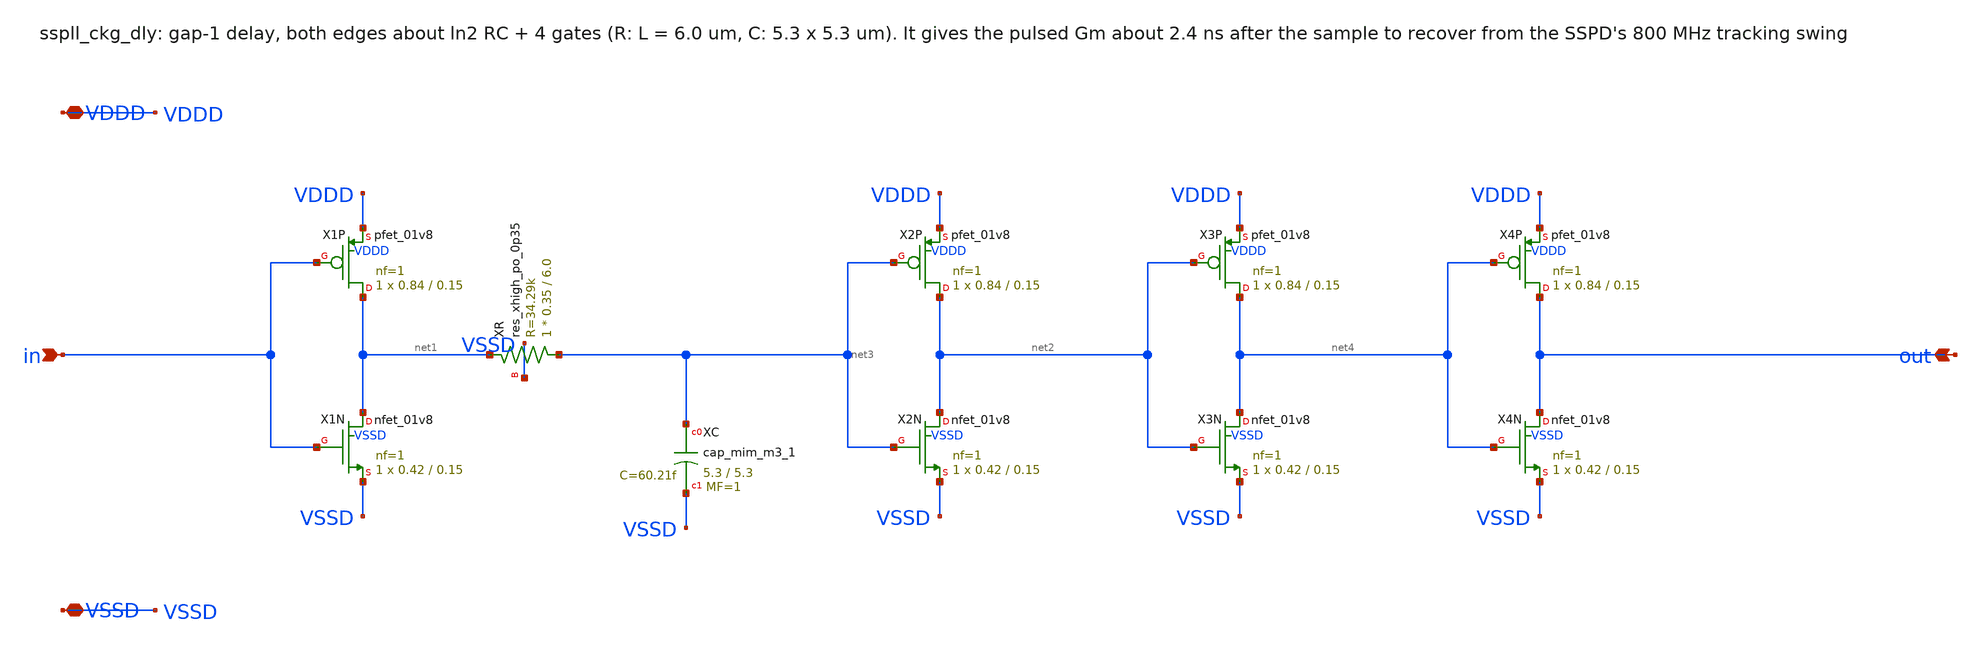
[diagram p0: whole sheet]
** sch_path: xschem/clkgen_hv/sspll_ckg_dly.sch
**.subckt sspll_ckg_dly in out VDDD VSSD
*.ipin in
*.opin out
*.iopin VDDD
*.iopin VSSD
XX1P net1 in VDDD VDDD sky130_fd_pr__pfet_01v8 L=0.15 W=0.84 nf=1 ad='int((nf+1)/2) * W/nf * 0.29' as='int((nf+2)/2) * W/nf * 0.29'
+ pd='2*int((nf+1)/2) * (W/nf + 0.29)' ps='2*int((nf+2)/2) * (W/nf + 0.29)' nrd='0.29 / W' nrs='0.29 / W'
+ sa=0 sb=0 sd=0 mult=1 m=1
XX1N net1 in VSSD VSSD sky130_fd_pr__nfet_01v8 L=0.15 W=0.42 nf=1 ad='int((nf+1)/2) * W/nf * 0.29' as='int((nf+2)/2) * W/nf * 0.29'
+ pd='2*int((nf+1)/2) * (W/nf + 0.29)' ps='2*int((nf+2)/2) * (W/nf + 0.29)' nrd='0.29 / W' nrs='0.29 / W'
+ sa=0 sb=0 sd=0 mult=1 m=1
XXR net3 net1 VSSD sky130_fd_pr__res_xhigh_po_0p35 L=6.0 mult=1 m=1
XXC net3 VSSD sky130_fd_pr__cap_mim_m3_1 W=5.3 L=5.3 MF=1 m=1
XX2P net2 net3 VDDD VDDD sky130_fd_pr__pfet_01v8 L=0.15 W=0.84 nf=1 ad='int((nf+1)/2) * W/nf * 0.29'
+ as='int((nf+2)/2) * W/nf * 0.29' pd='2*int((nf+1)/2) * (W/nf + 0.29)' ps='2*int((nf+2)/2) * (W/nf + 0.29)'
+ nrd='0.29 / W' nrs='0.29 / W' sa=0 sb=0 sd=0 mult=1 m=1
XX2N net2 net3 VSSD VSSD sky130_fd_pr__nfet_01v8 L=0.15 W=0.42 nf=1 ad='int((nf+1)/2) * W/nf * 0.29'
+ as='int((nf+2)/2) * W/nf * 0.29' pd='2*int((nf+1)/2) * (W/nf + 0.29)' ps='2*int((nf+2)/2) * (W/nf + 0.29)'
+ nrd='0.29 / W' nrs='0.29 / W' sa=0 sb=0 sd=0 mult=1 m=1
XX3P net4 net2 VDDD VDDD sky130_fd_pr__pfet_01v8 L=0.15 W=0.84 nf=1 ad='int((nf+1)/2) * W/nf * 0.29'
+ as='int((nf+2)/2) * W/nf * 0.29' pd='2*int((nf+1)/2) * (W/nf + 0.29)' ps='2*int((nf+2)/2) * (W/nf + 0.29)'
+ nrd='0.29 / W' nrs='0.29 / W' sa=0 sb=0 sd=0 mult=1 m=1
XX3N net4 net2 VSSD VSSD sky130_fd_pr__nfet_01v8 L=0.15 W=0.42 nf=1 ad='int((nf+1)/2) * W/nf * 0.29'
+ as='int((nf+2)/2) * W/nf * 0.29' pd='2*int((nf+1)/2) * (W/nf + 0.29)' ps='2*int((nf+2)/2) * (W/nf + 0.29)'
+ nrd='0.29 / W' nrs='0.29 / W' sa=0 sb=0 sd=0 mult=1 m=1
XX4P out net4 VDDD VDDD sky130_fd_pr__pfet_01v8 L=0.15 W=0.84 nf=1 ad='int((nf+1)/2) * W/nf * 0.29' as='int((nf+2)/2) * W/nf * 0.29'
+ pd='2*int((nf+1)/2) * (W/nf + 0.29)' ps='2*int((nf+2)/2) * (W/nf + 0.29)' nrd='0.29 / W' nrs='0.29 / W'
+ sa=0 sb=0 sd=0 mult=1 m=1
XX4N out net4 VSSD VSSD sky130_fd_pr__nfet_01v8 L=0.15 W=0.42 nf=1 ad='int((nf+1)/2) * W/nf * 0.29' as='int((nf+2)/2) * W/nf * 0.29'
+ pd='2*int((nf+1)/2) * (W/nf + 0.29)' ps='2*int((nf+2)/2) * (W/nf + 0.29)' nrd='0.29 / W' nrs='0.29 / W'
+ sa=0 sb=0 sd=0 mult=1 m=1
**.ends
.end
